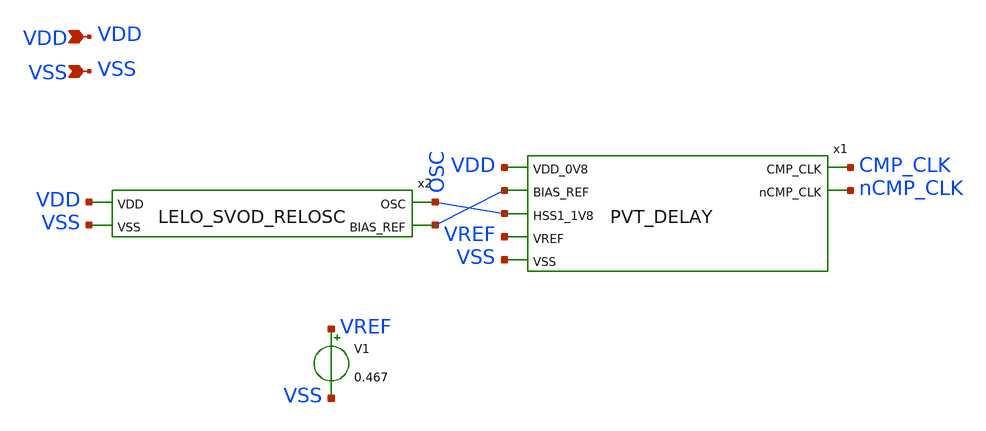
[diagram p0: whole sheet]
** sch_path: design/LELO_SVOD_SKY130A/PVT_DELAY_TB.sch
**.subckt PVT_DELAY_TB VDD VSS
*.ipin VDD
*.ipin VSS
x1 VDD net1 OSC CMP_CLK nCMP_CLK VREF VSS PVT_DELAY
x2 VDD OSC net1 VSS LELO_SVOD_RELOSC
V1 VREF VSS 0.467
**.ends
.end
